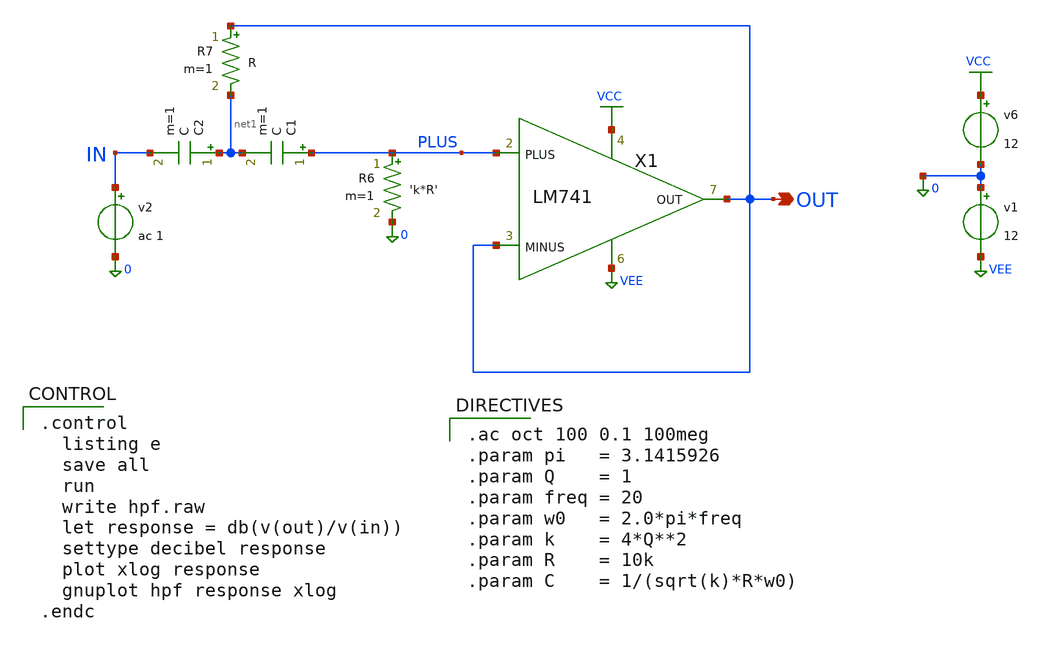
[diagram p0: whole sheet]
** sch_path: xschem_libraries_oa/ngspice/hpf_xschem/schematic/hpf_xschem.sch
* Copyright (C) 1998-2024 Stefan Frederik Schippers
* This program is free software; you can redistribute it and/or modify
* it under the terms of the GNU General Public License as published by
* the Free Software Foundation; either version 2 of the License, or
* (at your option) any later version.
* This program is distributed in the hope that it will be useful,
* but WITHOUT ANY WARRANTY; without even the implied warranty of
* MERCHANTABILITY or FITNESS FOR A PARTICULAR PURPOSE.  See the
* GNU General Public License for more details.
* You should have received a copy of the GNU General Public License
* along with this program; if not, write to the Free Software
**.subckt hpf_xschem OUT
*.opin OUT
v2 IN 0 ac 1
C1 PLUS net1 C m=1
R6 PLUS 0 'k*R' m=1
v6 VCC 0 12
v1 0 VEE 12
X1 PLUS OUT VCC VEE OUT LM741
R7 OUT net1 R m=1
C2 net1 IN C m=1
**** begin user architecture code

*//////////////////////////////////////////////////////////
*LM741 OPERATIONAL AMPLIFIER MACRO-MODEL
*//////////////////////////////////////////////////////////
*
* connections:      non-inverting input
*                   |   inverting input
*                   |   |   positive power supply
*                   |   |   |   negative power supply
*                   |   |   |   |   output
*                   |   |   |   |   |
*                   |   |   |   |   |
.SUBCKT LM741    1   2  99  50  28
*
*Features:
*Improved performance over industry standards
*Plug-in replacement for LM709,LM201,MC1439,748
*Input and output overload protection
*
****************INPUT STAGE**************
*
IOS 2 1 20N
*^Input offset current
R1 1 3 250K
R2 3 2 250K
I1 4 50 100U
R3 5 99 517
R4 6 99 517
Q1 5 2 4 QX
Q2 6 7 4 QX
*Fp2=2.55 MHz
C4 5 6 60.3614P
*
***********COMMON MODE EFFECT***********
*
I2 99 50 1.6MA
*^Quiescent supply current
EOS 7 1 POLY(1) 16 49 1E-3 1
*Input offset voltage.^
R8 99 49 40K
R9 49 50 40K
*
*********OUTPUT VOLTAGE LIMITING********
V2 99 8 1.63
D1 9 8 DX
D2 10 9 DX
V3 10 50 1.63
*
**************SECOND STAGE**************
*
EH 99 98 99 49 1
G1 98 9 5 6 2.1E-3
*Fp1=5 Hz
R5 98 9 95.493MEG
C3 98 9 333.33P
*
***************POLE STAGE***************
*
*Fp=30 MHz
G3 98 15 9 49 1E-6
R12 98 15 1MEG
C5 98 15 5.3052E-15
*
*********COMMON-MODE ZERO STAGE*********
*
*Fpcm=300 Hz
G4 98 16 3 49 3.1623E-8
L2 98 17 530.5M
R13 17 16 1K
*
**************OUTPUT STAGE**************
*
F6 50 99 POLY(1) V6 450U 1
E1 99 23 99 15 1
R16 24 23 25
D5 26 24 DX
V6 26 22 0.65V
R17 23 25 25
D6 25 27 DX
V7 22 27 0.65V
V5 22 21 0.18V
D4 21 15 DX
V4 20 22 0.18V
D3 15 20 DX
L3 22 28 100P
RL3 22 28 100K
*
***************MODELS USED**************
*
.MODEL DX D(IS=1E-15)
.MODEL QX NPN(BF=625)
*
.ENDS


**** end user architecture code
**.ends
.GLOBAL VEE
.GLOBAL VCC
**** begin user architecture code

.control
  listing e
  save all
  run
  write hpf.raw
  let response = db(v(out)/v(in))
  settype decibel response
  plot xlog response
  gnuplot hpf response xlog
.endc



.ac oct 100 0.1 100meg
.param pi   = 3.1415926
.param Q    = 1
.param freq = 20
.param w0   = 2.0*pi*freq
.param k    = 4*Q**2
.param R    = 10k
.param C    = 1/(sqrt(k)*R*w0)


**** end user architecture code
.end
